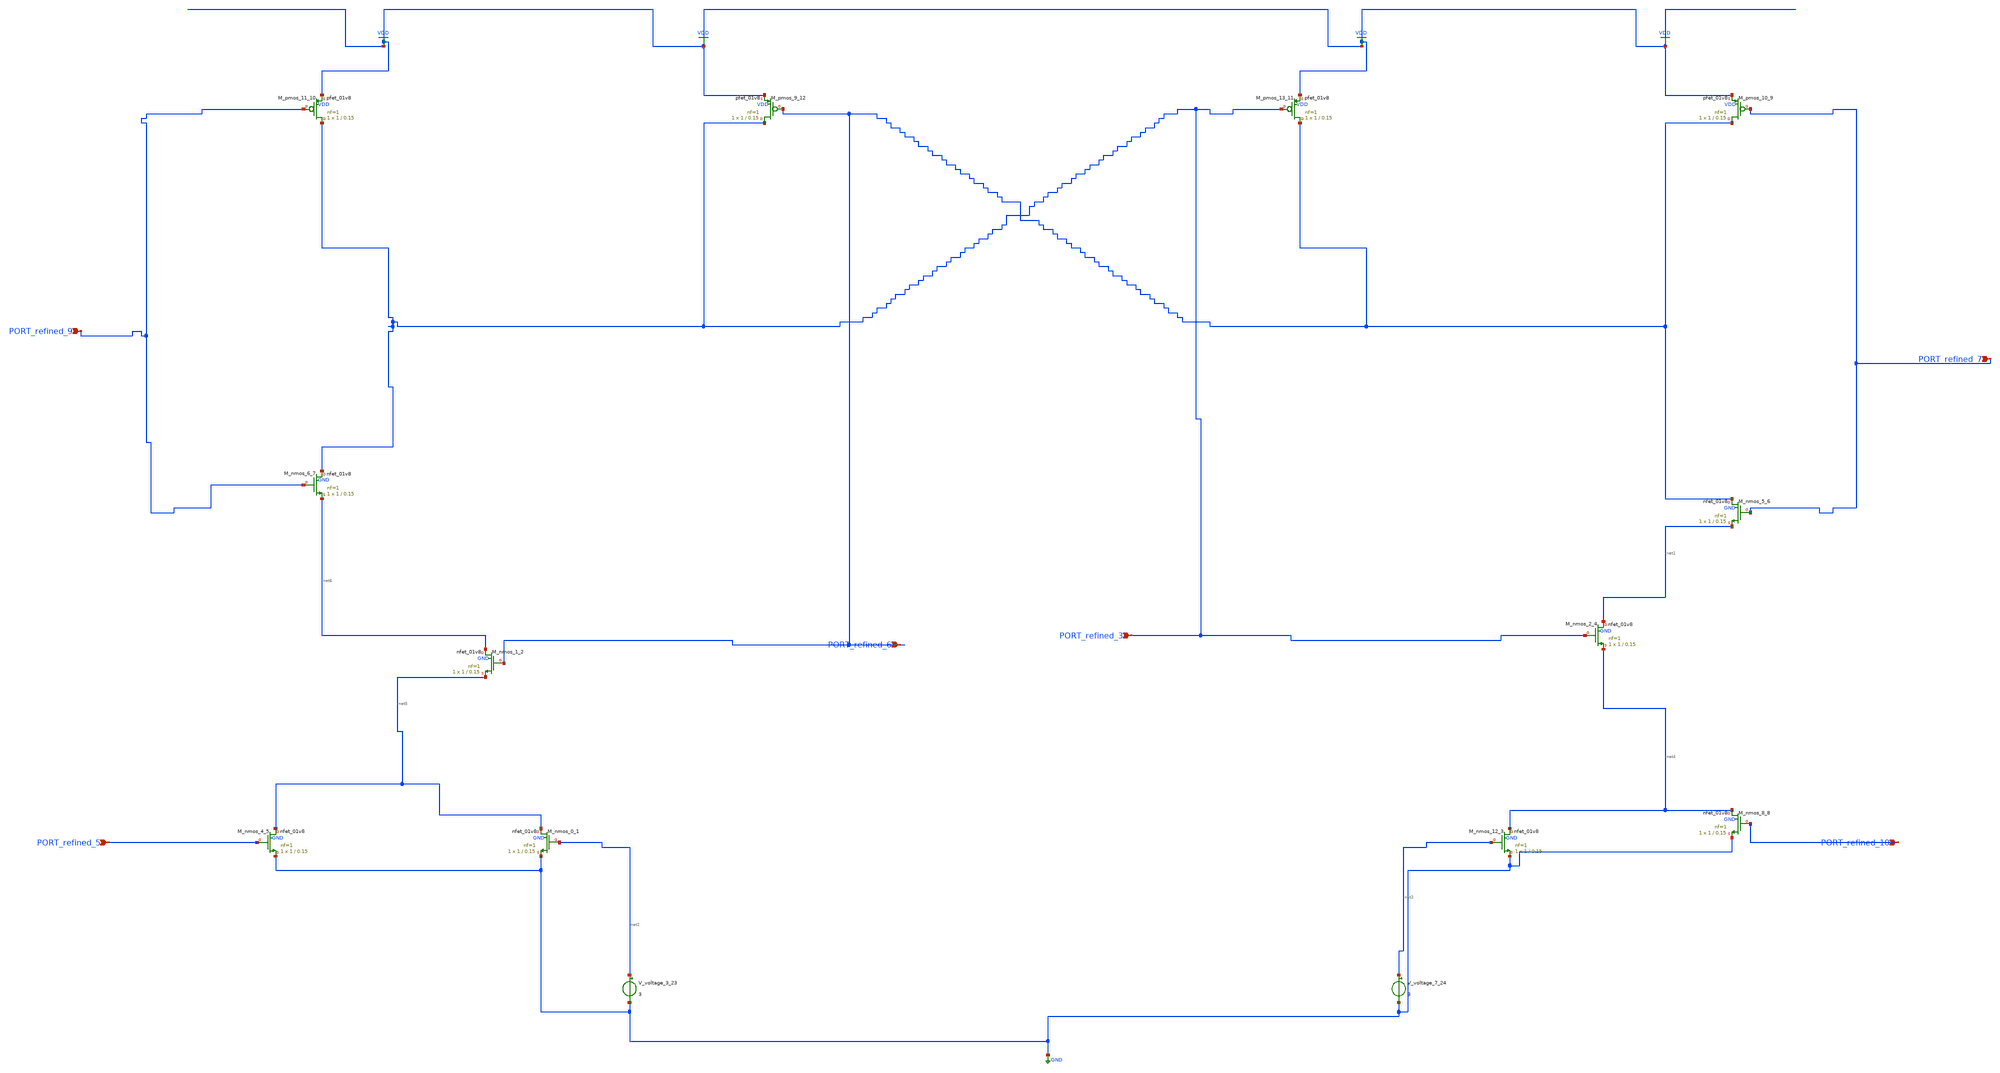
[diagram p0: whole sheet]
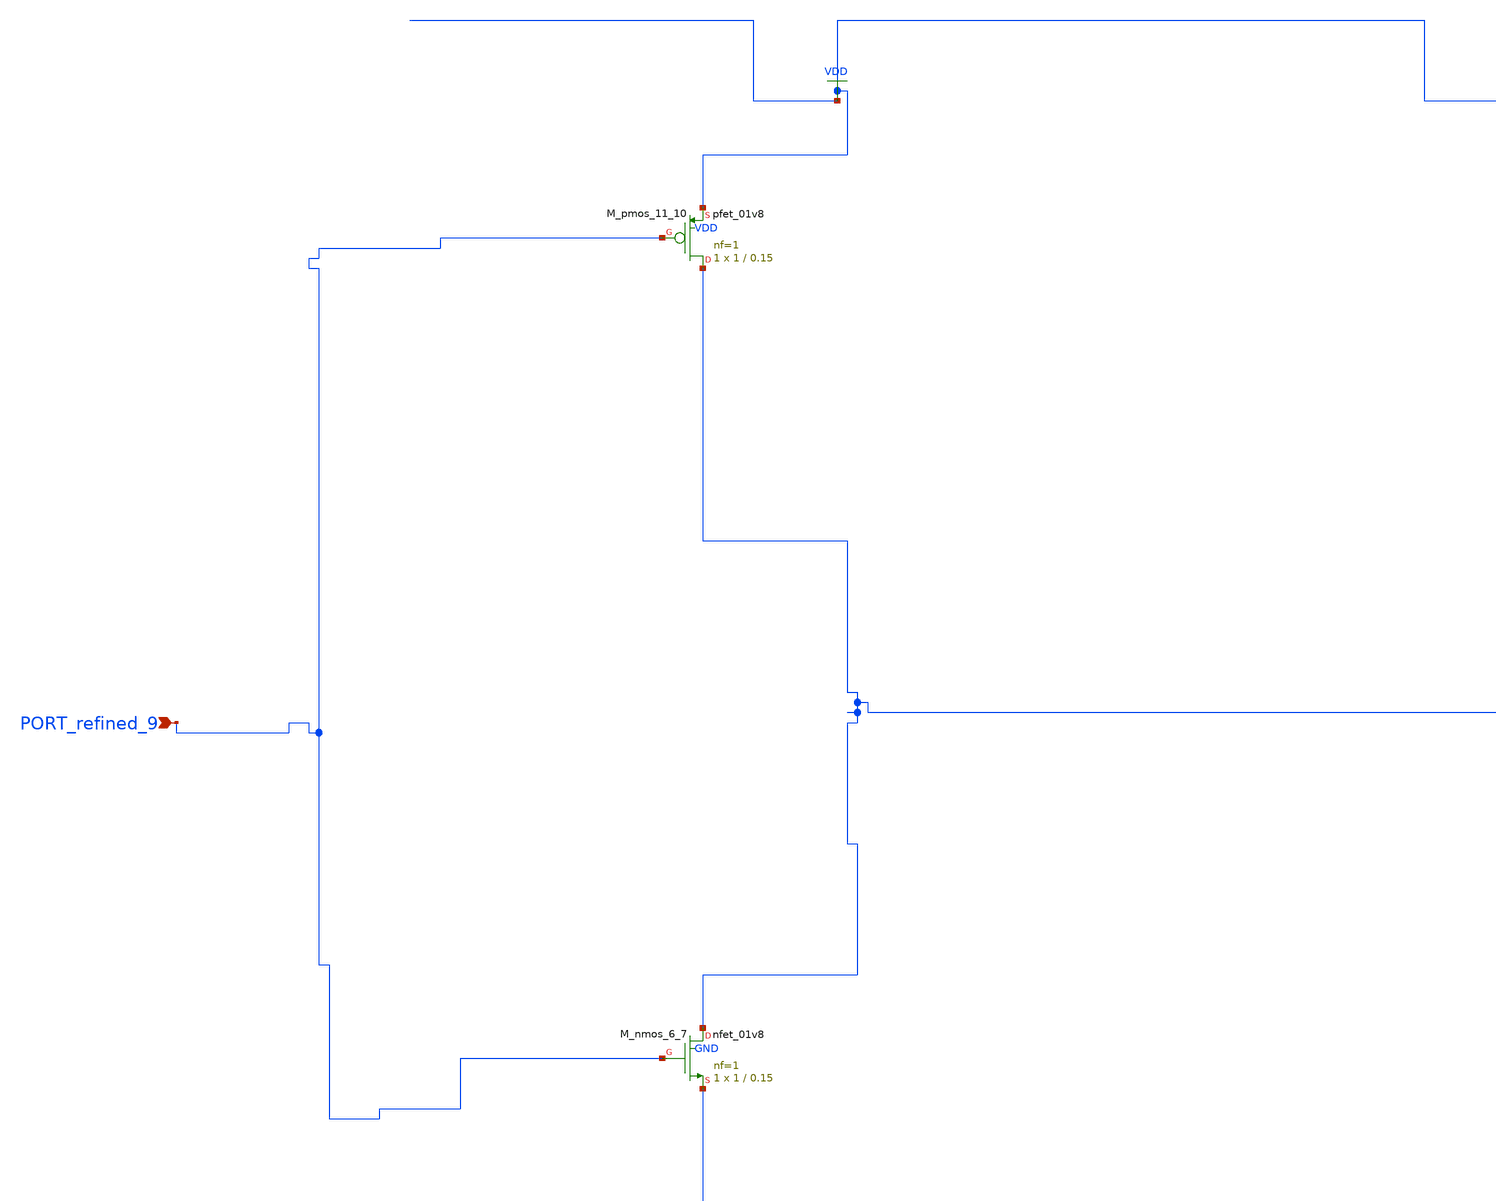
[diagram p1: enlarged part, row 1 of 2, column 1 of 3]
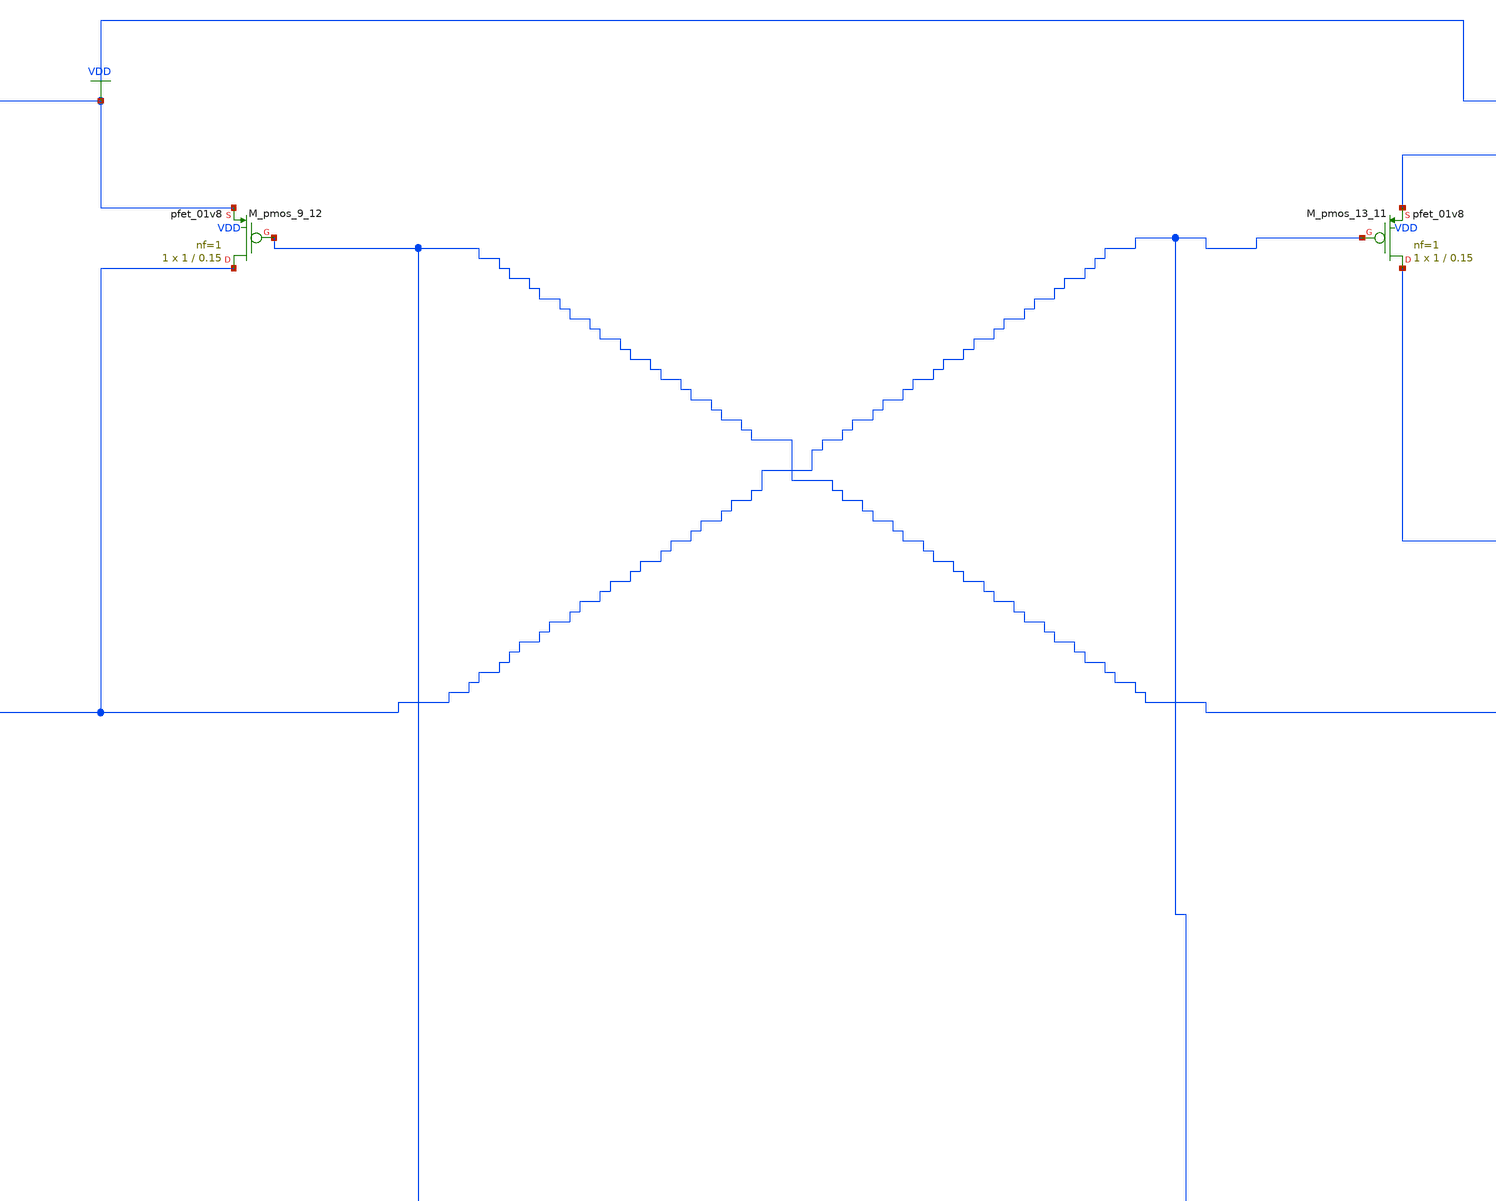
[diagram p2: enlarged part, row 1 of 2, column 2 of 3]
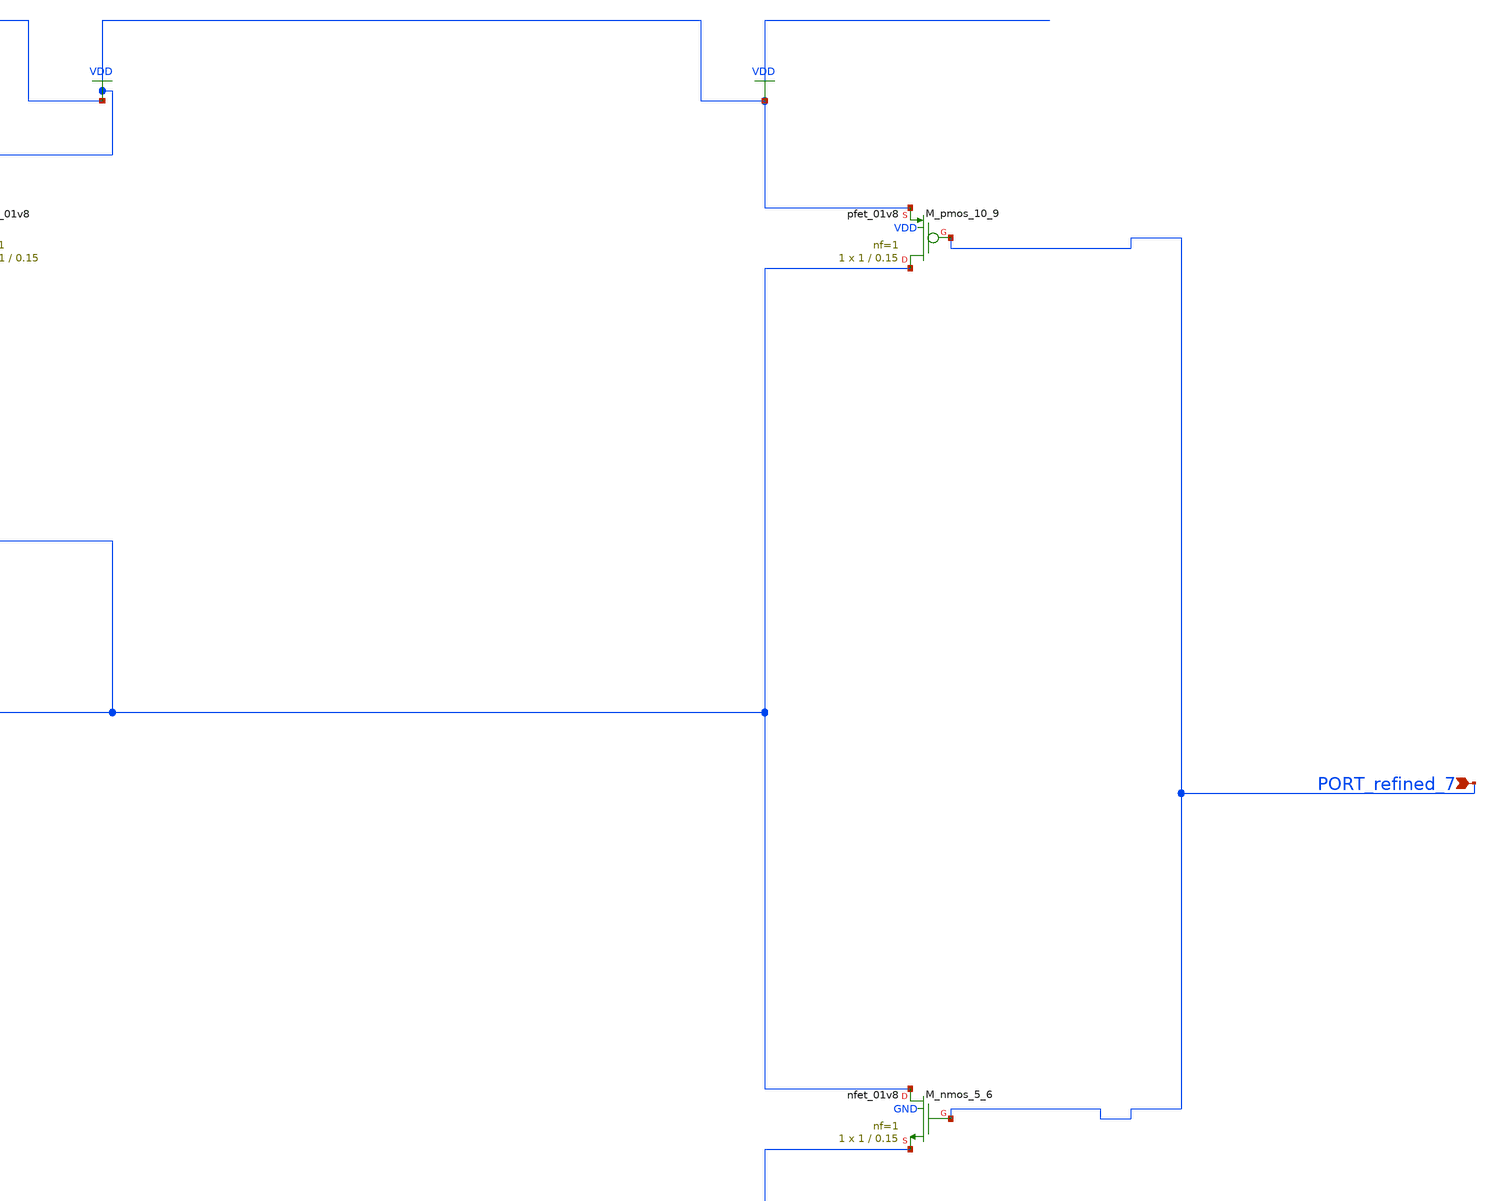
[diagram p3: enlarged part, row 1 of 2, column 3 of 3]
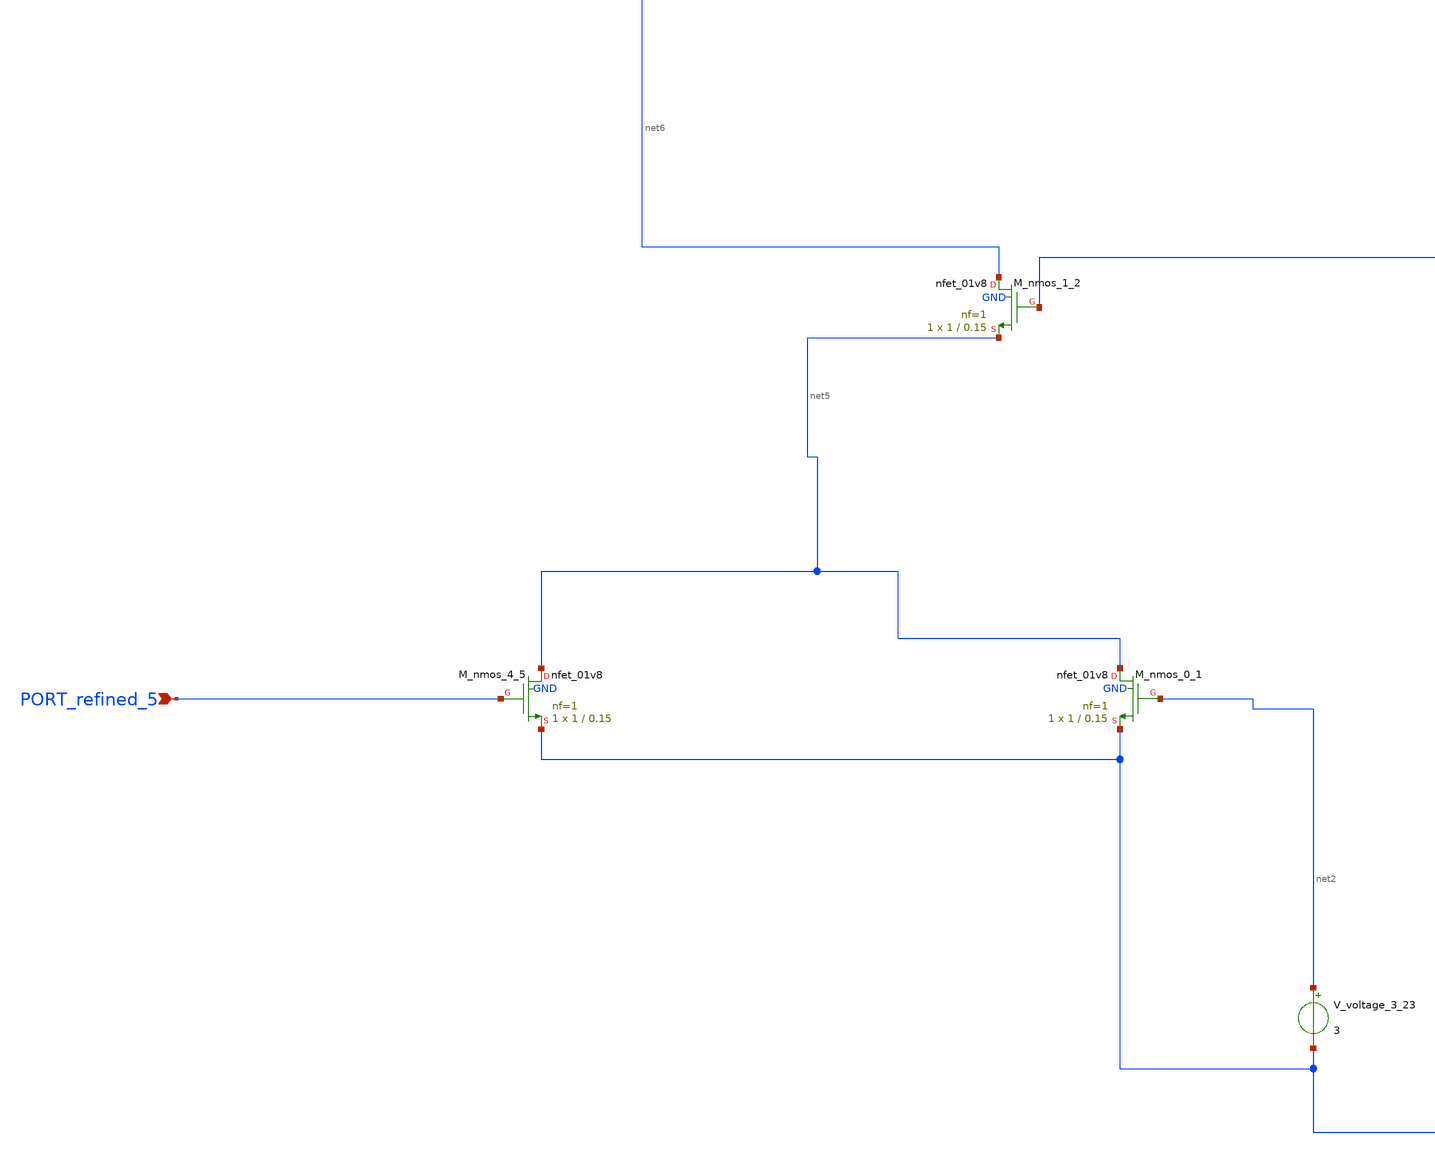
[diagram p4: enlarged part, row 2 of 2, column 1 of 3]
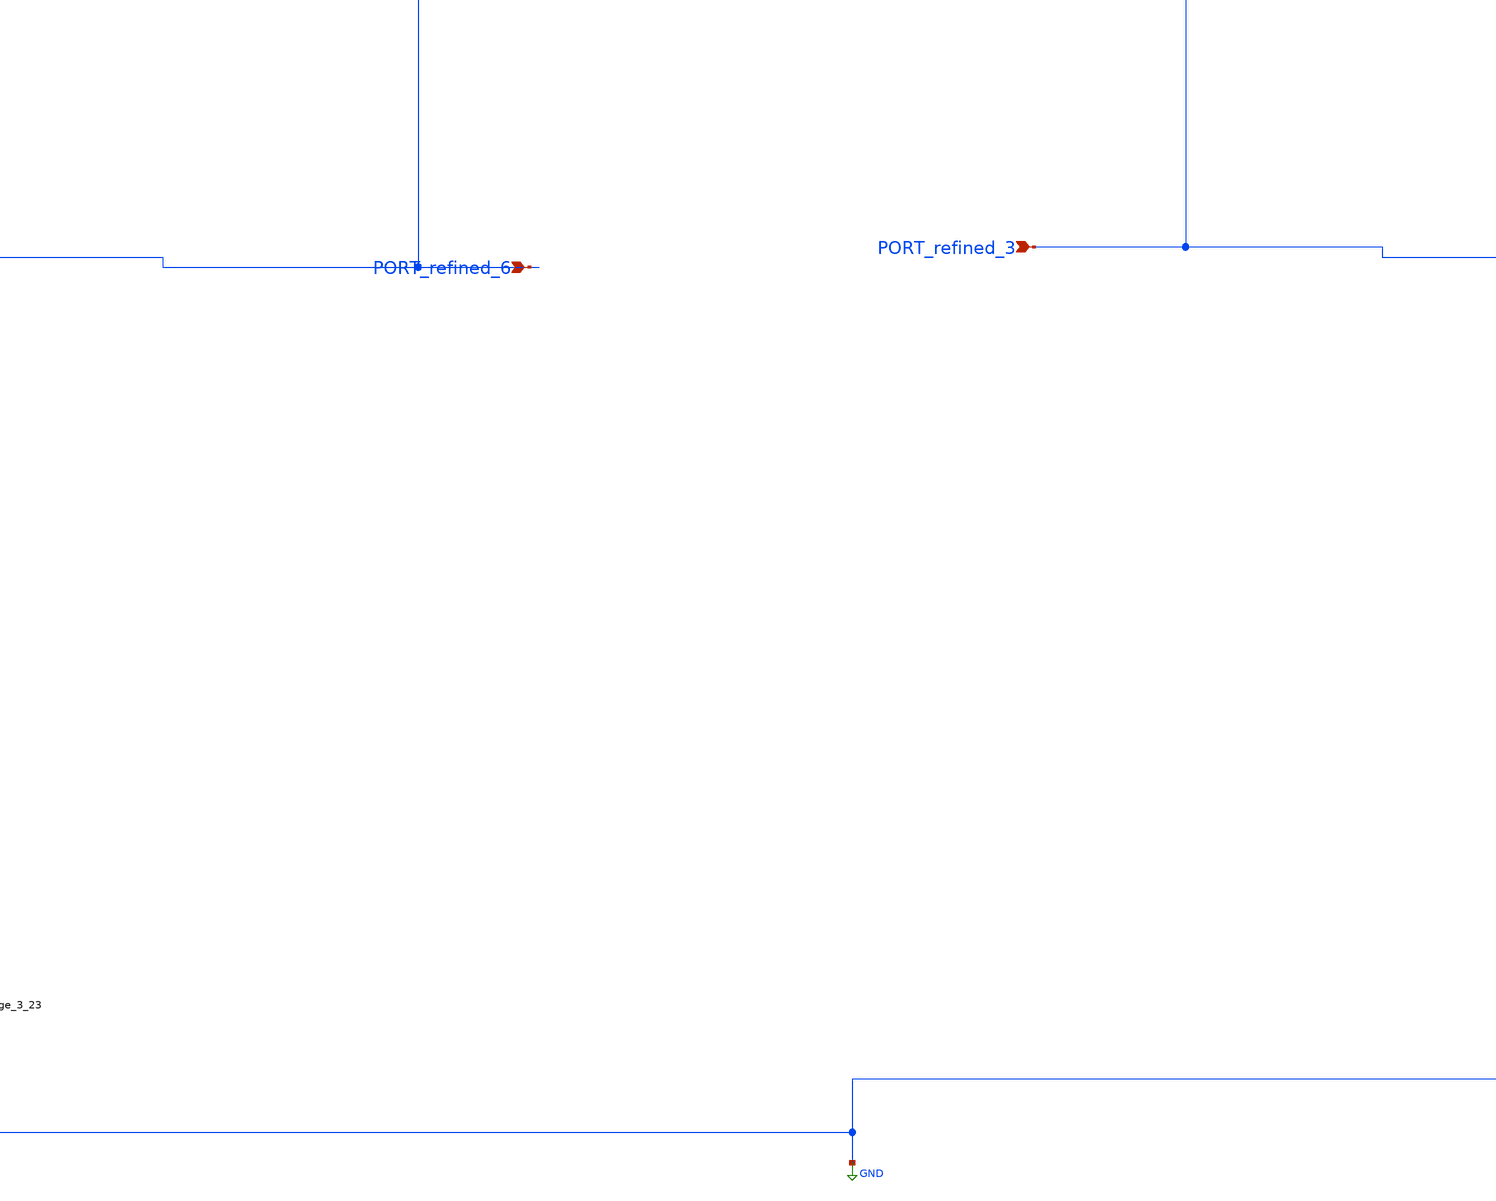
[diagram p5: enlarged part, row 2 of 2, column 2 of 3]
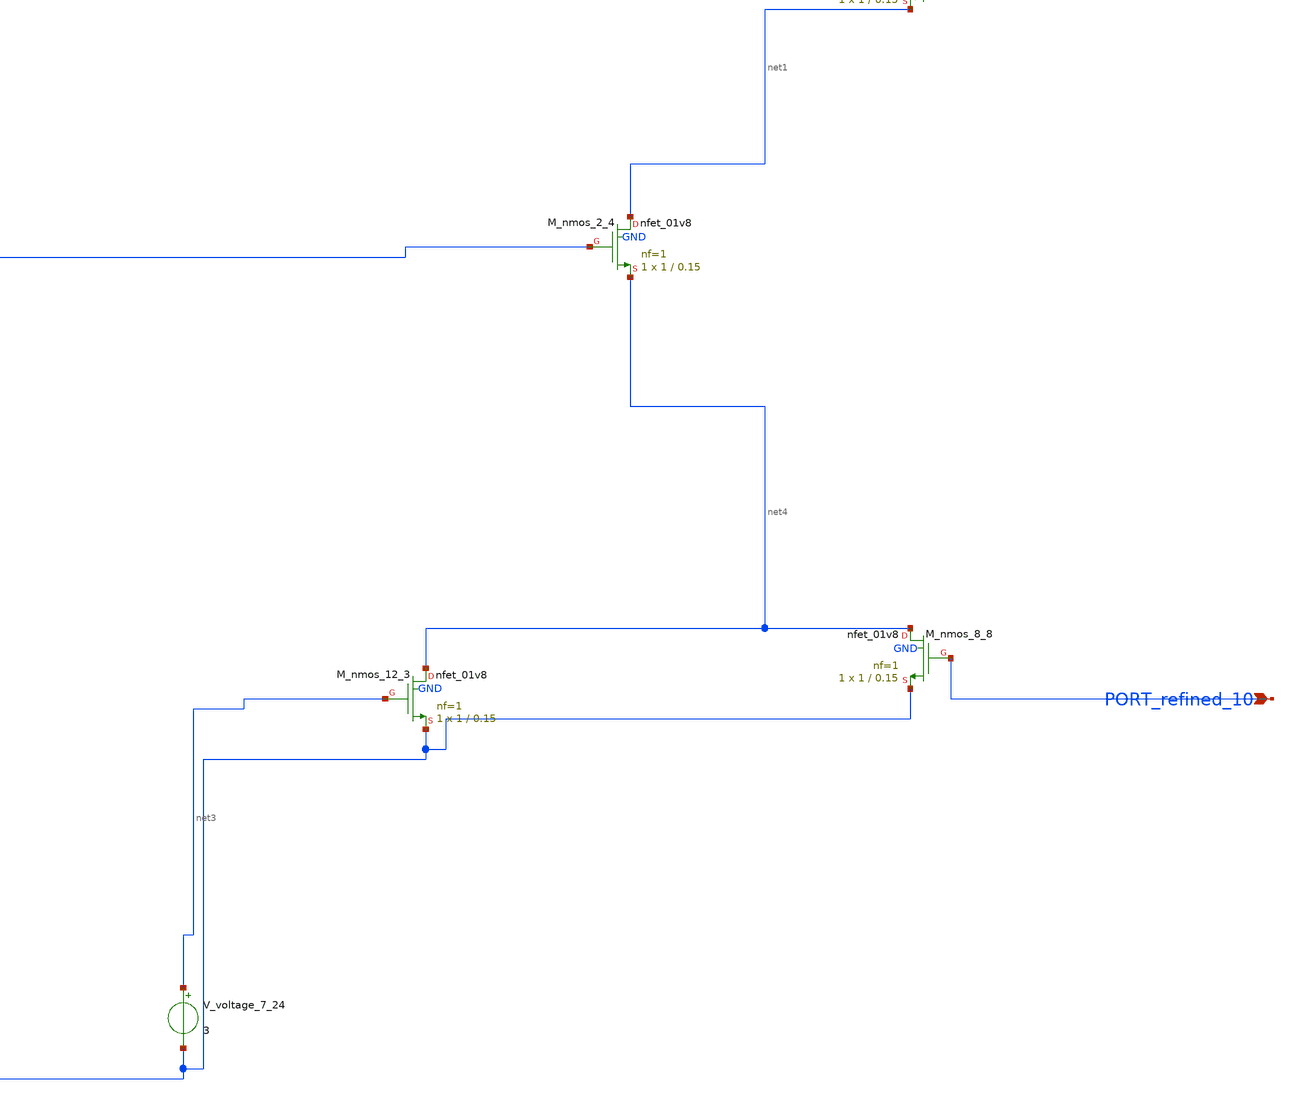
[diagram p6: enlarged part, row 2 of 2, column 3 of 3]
** sch_path: schematics/Image2Net/127.sch
**.subckt 127 PORT_refined_7 PORT_refined_6 PORT_refined_9 PORT_refined_3 PORT_refined_5
*+ PORT_refined_10
*.ipin PORT_refined_7
*.ipin PORT_refined_6
*.ipin PORT_refined_9
*.ipin PORT_refined_3
*.ipin PORT_refined_5
*.ipin PORT_refined_10
XM_nmos_0_1 net5 net2 GND GND sky130_fd_pr__nfet_01v8 L=0.15 W=1 nf=1 ad='int((1 + 1)/2) * 1 / 1 * 0.29'
+ as='int((1 + 2)/2) * 1 / 1 * 0.29' pd='2*int((1 + 1)/2) * (1 / 1 + 0.29)' ps='2*int((1 + 2)/2) * (1 / 1 + 0.29)'
+ nrd='0.29 / 1 ' nrs='0.29 / 1 ' sa=0 sb=0 sd=0 mult=1 m=1
XM_nmos_1_2 net6 PORT_refined_6 net5 GND sky130_fd_pr__nfet_01v8 L=0.15 W=1 nf=1 ad='int((1 + 1)/2) * 1 / 1 * 0.29'
+ as='int((1 + 2)/2) * 1 / 1 * 0.29' pd='2*int((1 + 1)/2) * (1 / 1 + 0.29)' ps='2*int((1 + 2)/2) * (1 / 1 + 0.29)'
+ nrd='0.29 / 1 ' nrs='0.29 / 1 ' sa=0 sb=0 sd=0 mult=1 m=1
XM_nmos_12_3 net4 net3 GND GND sky130_fd_pr__nfet_01v8 L=0.15 W=1 nf=1 ad='int((1 + 1)/2) * 1 / 1 * 0.29'
+ as='int((1 + 2)/2) * 1 / 1 * 0.29' pd='2*int((1 + 1)/2) * (1 / 1 + 0.29)' ps='2*int((1 + 2)/2) * (1 / 1 + 0.29)'
+ nrd='0.29 / 1 ' nrs='0.29 / 1 ' sa=0 sb=0 sd=0 mult=1 m=1
XM_nmos_2_4 net1 PORT_refined_3 net4 GND sky130_fd_pr__nfet_01v8 L=0.15 W=1 nf=1 ad='int((1 + 1)/2) * 1 / 1 * 0.29'
+ as='int((1 + 2)/2) * 1 / 1 * 0.29' pd='2*int((1 + 1)/2) * (1 / 1 + 0.29)' ps='2*int((1 + 2)/2) * (1 / 1 + 0.29)'
+ nrd='0.29 / 1 ' nrs='0.29 / 1 ' sa=0 sb=0 sd=0 mult=1 m=1
XM_nmos_4_5 net5 PORT_refined_5 GND GND sky130_fd_pr__nfet_01v8 L=0.15 W=1 nf=1 ad='int((1 + 1)/2) * 1 / 1 * 0.29'
+ as='int((1 + 2)/2) * 1 / 1 * 0.29' pd='2*int((1 + 1)/2) * (1 / 1 + 0.29)' ps='2*int((1 + 2)/2) * (1 / 1 + 0.29)'
+ nrd='0.29 / 1 ' nrs='0.29 / 1 ' sa=0 sb=0 sd=0 mult=1 m=1
XM_nmos_5_6 PORT_refined_6 PORT_refined_7 net1 GND sky130_fd_pr__nfet_01v8 L=0.15 W=1 nf=1 ad='int((1 + 1)/2) * 1 / 1 * 0.29'
+ as='int((1 + 2)/2) * 1 / 1 * 0.29' pd='2*int((1 + 1)/2) * (1 / 1 + 0.29)' ps='2*int((1 + 2)/2) * (1 / 1 + 0.29)'
+ nrd='0.29 / 1 ' nrs='0.29 / 1 ' sa=0 sb=0 sd=0 mult=1 m=1
XM_nmos_6_7 PORT_refined_3 PORT_refined_9 net6 GND sky130_fd_pr__nfet_01v8 L=0.15 W=1 nf=1 ad='int((1 + 1)/2) * 1 / 1 * 0.29'
+ as='int((1 + 2)/2) * 1 / 1 * 0.29' pd='2*int((1 + 1)/2) * (1 / 1 + 0.29)' ps='2*int((1 + 2)/2) * (1 / 1 + 0.29)'
+ nrd='0.29 / 1 ' nrs='0.29 / 1 ' sa=0 sb=0 sd=0 mult=1 m=1
XM_nmos_8_8 net4 PORT_refined_10 GND GND sky130_fd_pr__nfet_01v8 L=0.15 W=1 nf=1 ad='int((1 + 1)/2) * 1 / 1 * 0.29'
+ as='int((1 + 2)/2) * 1 / 1 * 0.29' pd='2*int((1 + 1)/2) * (1 / 1 + 0.29)' ps='2*int((1 + 2)/2) * (1 / 1 + 0.29)'
+ nrd='0.29 / 1 ' nrs='0.29 / 1 ' sa=0 sb=0 sd=0 mult=1 m=1
XM_pmos_10_9 PORT_refined_6 PORT_refined_7 VDD VDD sky130_fd_pr__pfet_01v8 L=0.15 W=1 nf=1 ad='int((1 + 1)/2) * 1 / 1 * 0.29'
+ as='int((1 + 2)/2) * 1 / 1 * 0.29' pd='2*int((1 + 1)/2) * (1 / 1 + 0.29)' ps='2*int((1 + 2)/2) * (1 / 1 + 0.29)'
+ nrd='0.29 / 1 ' nrs='0.29 / 1 ' sa=0 sb=0 sd=0 mult=1 m=1
XM_pmos_11_10 PORT_refined_3 PORT_refined_9 VDD VDD sky130_fd_pr__pfet_01v8 L=0.15 W=1 nf=1 ad='int((1 + 1)/2) * 1 / 1 * 0.29'
+ as='int((1 + 2)/2) * 1 / 1 * 0.29' pd='2*int((1 + 1)/2) * (1 / 1 + 0.29)' ps='2*int((1 + 2)/2) * (1 / 1 + 0.29)'
+ nrd='0.29 / 1 ' nrs='0.29 / 1 ' sa=0 sb=0 sd=0 mult=1 m=1
XM_pmos_13_11 PORT_refined_6 PORT_refined_3 VDD VDD sky130_fd_pr__pfet_01v8 L=0.15 W=1 nf=1 ad='int((1 + 1)/2) * 1 / 1 * 0.29'
+ as='int((1 + 2)/2) * 1 / 1 * 0.29' pd='2*int((1 + 1)/2) * (1 / 1 + 0.29)' ps='2*int((1 + 2)/2) * (1 / 1 + 0.29)'
+ nrd='0.29 / 1 ' nrs='0.29 / 1 ' sa=0 sb=0 sd=0 mult=1 m=1
XM_pmos_9_12 PORT_refined_3 PORT_refined_6 VDD VDD sky130_fd_pr__pfet_01v8 L=0.15 W=1 nf=1 ad='int((1 + 1)/2) * 1 / 1 * 0.29'
+ as='int((1 + 2)/2) * 1 / 1 * 0.29' pd='2*int((1 + 1)/2) * (1 / 1 + 0.29)' ps='2*int((1 + 2)/2) * (1 / 1 + 0.29)'
+ nrd='0.29 / 1 ' nrs='0.29 / 1 ' sa=0 sb=0 sd=0 mult=1 m=1
V_voltage_3_23 net2 GND 3
V_voltage_7_24 net3 GND 3
**.ends
.GLOBAL GND
.GLOBAL VDD
.end
